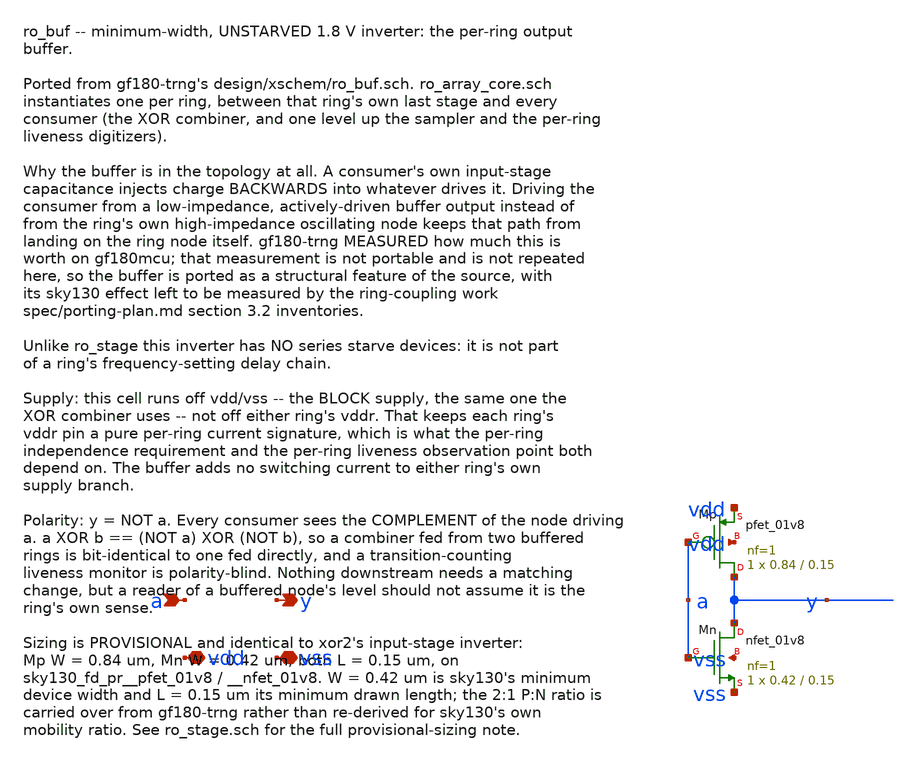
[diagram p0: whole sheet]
** sch_path: design/xschem/ro_buf.sch
**.subckt ro_buf a y vdd vss
*.ipin a
*.opin y
*.iopin vdd
*.iopin vss
XMp y a vdd vdd sky130_fd_pr__pfet_01v8 L=0.15 W=0.84 nf=1 ad='int((nf+1)/2) * W/nf * 0.29' as='int((nf+2)/2) * W/nf * 0.29'
+ pd='2*int((nf+1)/2) * (W/nf + 0.29)' ps='2*int((nf+2)/2) * (W/nf + 0.29)' nrd='0.29 / W' nrs='0.29 / W'
+ sa=0 sb=0 sd=0 mult=1 m=1
XMn y a vss vss sky130_fd_pr__nfet_01v8 L=0.15 W=0.42 nf=1 ad='int((1 + 1)/2) * 0.42 / 1 * 0.29' as='int((1 + 2)/2) * 0.42 / 1 * 0.29'
+ pd='2*int((1 + 1)/2) * (0.42 / 1 + 0.29)' ps='2*int((1 + 2)/2) * (0.42 / 1 + 0.29)' nrd='0.29 / 0.42 '
+ nrs='0.29 / 0.42 ' sa=0 sb=0 sd=0 mult=1 m=1
**.ends
.end
